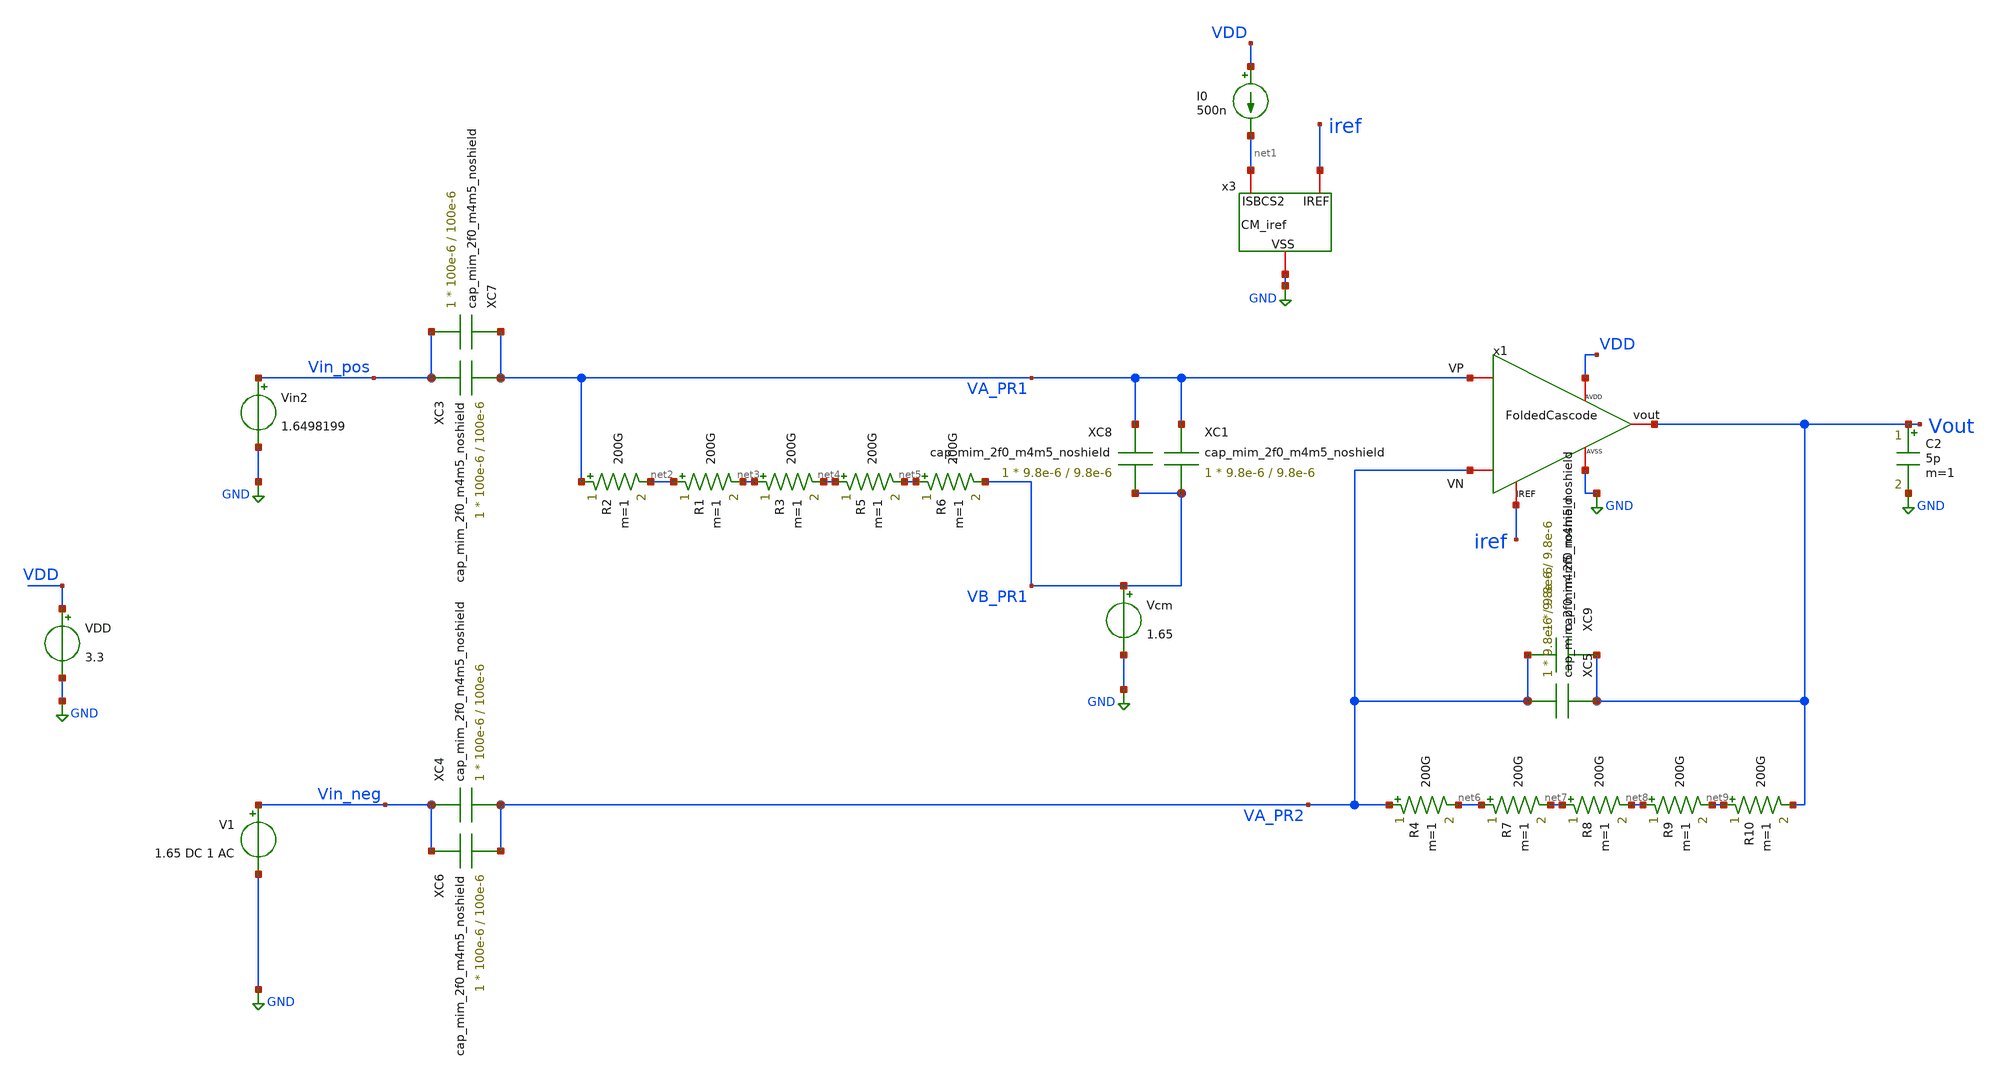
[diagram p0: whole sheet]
** sch_path: TIA_Filter/TB_filter_noPR_ac.sch
**.subckt TB_filter_noPR_ac
VDD VDD GND 3.3
C2 Vout GND 5p m=1
x1 VA_PR1 VA_PR2 Vout iref VDD GND FoldedCascode
I0 VDD net1 500n
Vcm VB_PR1 GND 1.65
R2 VA_PR1 net2 200G m=1
XC1 VA_PR1 VB_PR1 cap_mim_2f0_m4m5_noshield c_width=9.8e-6 c_length=9.8e-6 m=1
XC5 Vout VA_PR2 cap_mim_2f0_m4m5_noshield c_width=9.8e-6 c_length=9.8e-6 m=1
XC3 Vin_pos VA_PR1 cap_mim_2f0_m4m5_noshield c_width=100e-6 c_length=100e-6 m=1
XC4 Vin_neg VA_PR2 cap_mim_2f0_m4m5_noshield c_width=100e-6 c_length=100e-6 m=1
x3 net1 iref GND CM_iref
Vin2 Vin_pos GND 1.6498199
V1 Vin_neg GND 1.65 DC 1 AC
R1 net2 net3 200G m=1
R3 net3 net4 200G m=1
R5 net4 net5 200G m=1
R6 net5 VB_PR1 200G m=1
R4 VA_PR2 net6 200G m=1
R7 net6 net7 200G m=1
R8 net7 net8 200G m=1
R9 net8 net9 200G m=1
R10 net9 Vout 200G m=1
XC6 Vin_neg VA_PR2 cap_mim_2f0_m4m5_noshield c_width=100e-6 c_length=100e-6 m=1
XC7 VA_PR1 Vin_pos cap_mim_2f0_m4m5_noshield c_width=100e-6 c_length=100e-6 m=1
XC8 VA_PR1 VB_PR1 cap_mim_2f0_m4m5_noshield c_width=9.8e-6 c_length=9.8e-6 m=1
XC9 Vout VA_PR2 cap_mim_2f0_m4m5_noshield c_width=9.8e-6 c_length=9.8e-6 m=1
**** begin user architecture code

.include $::180MCU_MODELS/design.ngspice
.lib $::180MCU_MODELS/sm141064.ngspice typical
.lib $::180MCU_MODELS/sm141064.ngspice cap_mim
.lib $::180MCU_MODELS/sm141064.ngspice res_typical
.lib $::180MCU_MODELS/sm141064.ngspice moscap_typical
.lib $::180MCU_MODELS/sm141064.ngspice mimcap_typical



.option gmin=1e-14
*.option abstol=1e-2
.option klu

.control
save all

*op
*remzerovec
*write TB_filter_noPR_ac.raw
*set appendwrite

ac dec 10 1m 1e8
remzerovec
write TB_filter_noPR_ac.raw
wrdata /home/gmaranhao/Desktop/Bracolin/TIA_Filter/FilterPlots/Filter_noPR_AC_TT.txt V(Vout)
set appendwrite

.endc


**** end user architecture code
**.ends
.GLOBAL GND
.end
